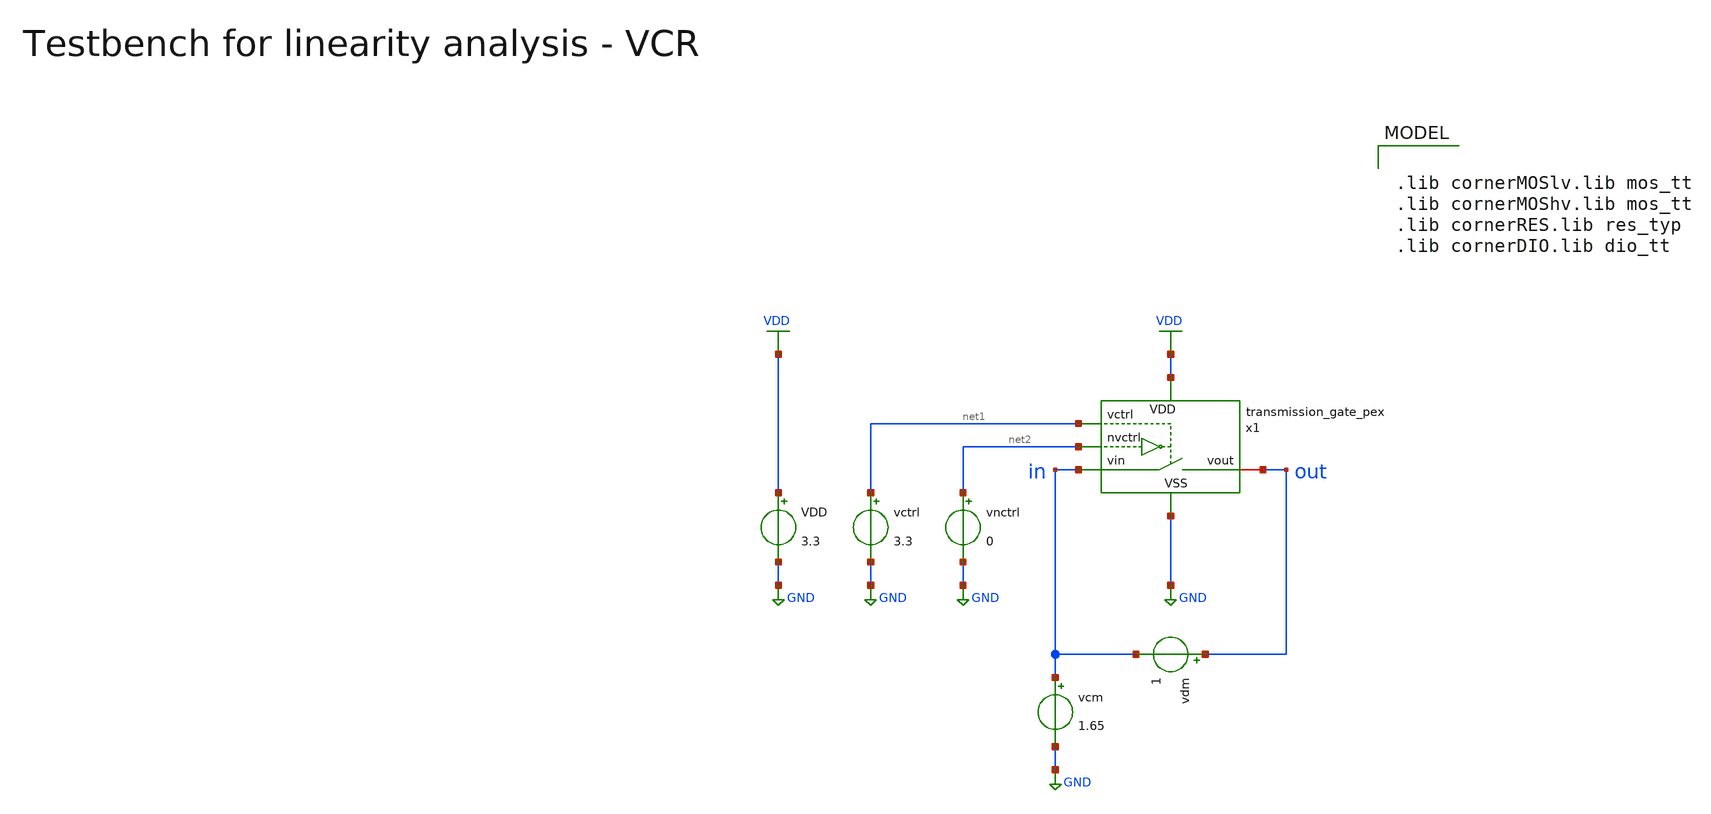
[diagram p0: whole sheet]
** sch_path: macros/heichips26_vcr/macros/switched_capacitor/testbenches/xschem/tb_transmission_gate_pex_linearity_dc.sch
**.subckt tb_transmission_gate_pex_linearity_dc
VDD VDD GND 3.3
vcm in GND 1.65
vctrl net1 GND 3.3
vnctrl net2 GND 0
vdm out in 1
x1 net1 in out net2 VDD GND transmission_gate_pex
**** begin user architecture code

.lib cornerMOSlv.lib mos_tt
.lib cornerMOShv.lib mos_tt
.lib cornerRES.lib res_typ
.lib cornerDIO.lib dio_tt



.include ../../../netlist/pex/transmission_gate_magic_pex_3.spice

.param temp=27

* Derived timing parameters

.options savecurrents klu method=gear reltol=1e-3 abstol=1e-15 gmin=1e-15
.probe alli
.control

unset appendwrite
set wr_vecnames
set wr_singlescale

echo
echo # ------------------------------------------------------------------------------
echo # VCM sweep:
echo # ------------------------------------------------------------------------------
echo

dc vcm -1 3.3 0.05 vdm 0.1 2.1 0.5
let vcm = (out+in)/2
let R = (in-out)/i(vdm)
plot R vs vcm
wrdata ../plot_simulations/data/@schname\_vcm.txt in out i(vdm)

echo
echo # ------------------------------------------------------------------------------
echo # VDM sweep:
echo # ------------------------------------------------------------------------------
echo

dc vdm -3.3 3.3 0.052 vcm 0.65 2.65 0.5
let vdm = out-in
let R = (in-out)/i(vdm)
plot R vs vdm
wrdata ../plot_simulations/data/@schname\_vdm.txt in out i(vdm)

.endc


**** end user architecture code
**.ends
.GLOBAL GND
.GLOBAL VDD
.end
